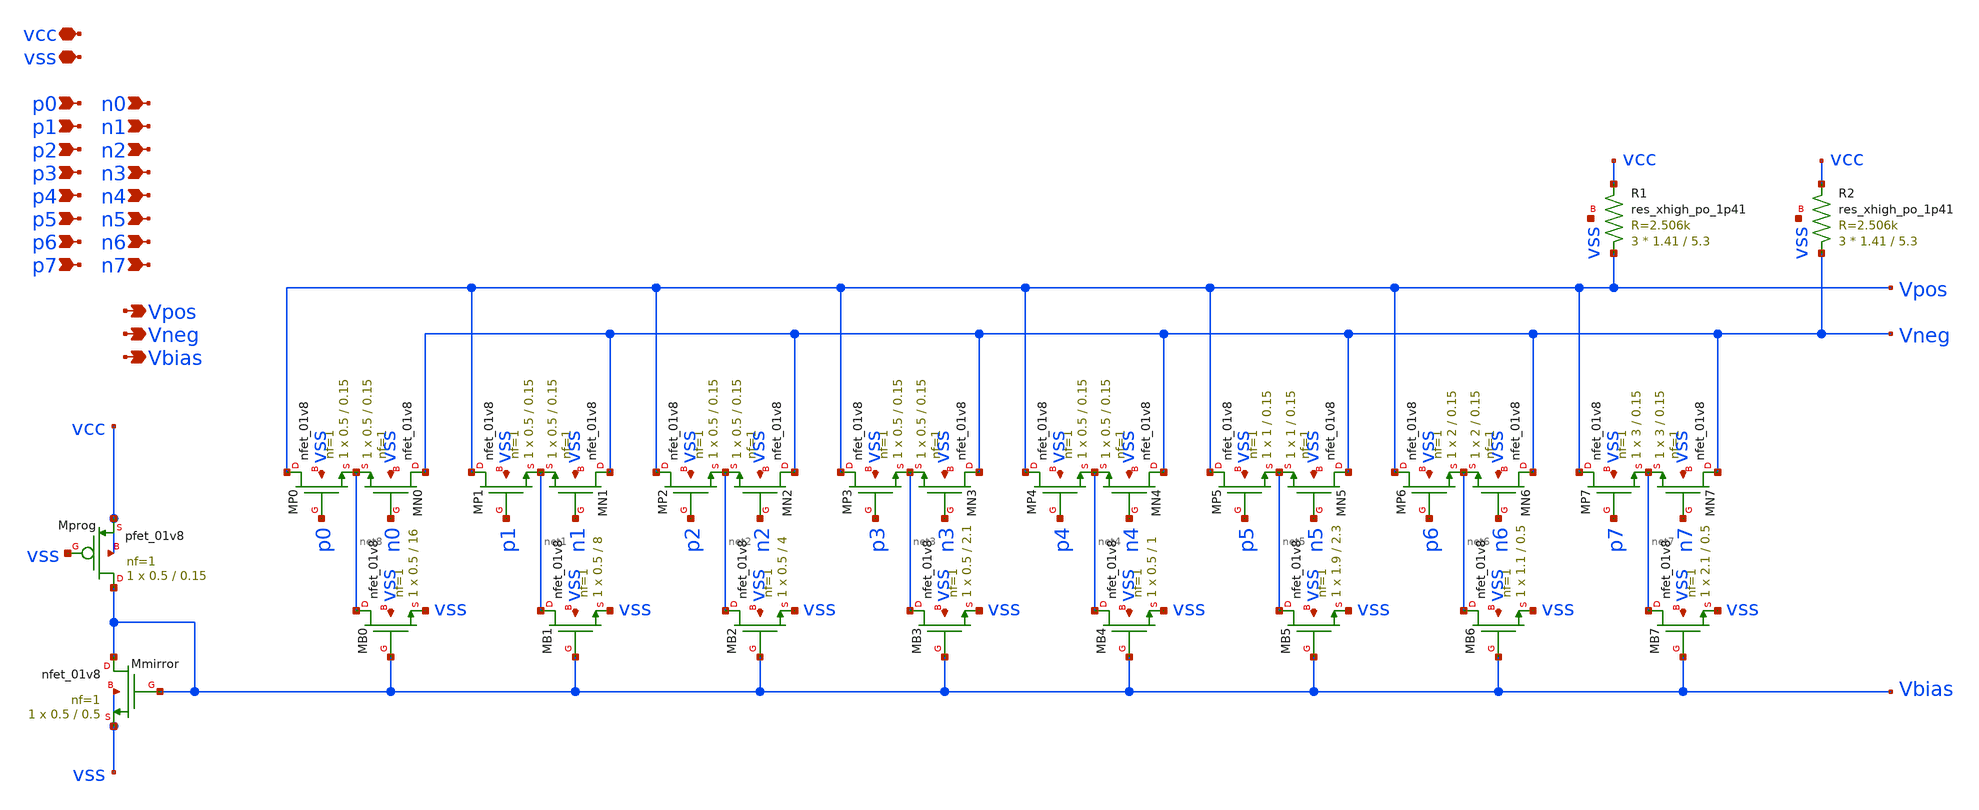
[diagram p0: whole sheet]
** sch_path: xschem/csdac.sch
**.subckt csdac vcc vss p0 n0 p1 n1 p2 n2 p3 n3 p4 n4 p5 n5 p6 n6 p7 n7 Vpos Vneg Vbias
*.iopin vcc
*.iopin vss
*.ipin p0
*.ipin n0
*.ipin p1
*.ipin n1
*.ipin p2
*.ipin n2
*.ipin p3
*.ipin n3
*.ipin p4
*.ipin n4
*.ipin p5
*.ipin n5
*.ipin p6
*.ipin n6
*.ipin p7
*.ipin n7
*.opin Vpos
*.opin Vneg
*.opin Vbias
XMprog Vbias vss vcc vcc sky130_fd_pr__pfet_01v8 L=0.15 W=0.5 nf=1 ad='int((nf+1)/2) * W/nf * 0.29' as='int((nf+2)/2) * W/nf * 0.29'
+ pd='2*int((nf+1)/2) * (W/nf + 0.29)' ps='2*int((nf+2)/2) * (W/nf + 0.29)' nrd='0.29 / W' nrs='0.29 / W'
+ sa=0 sb=0 sd=0 mult=1 m=1
XMmirror Vbias Vbias vss vss sky130_fd_pr__nfet_01v8 L=0.5 W=0.5 nf=1 ad='int((nf+1)/2) * W/nf * 0.29'
+ as='int((nf+2)/2) * W/nf * 0.29' pd='2*int((nf+1)/2) * (W/nf + 0.29)' ps='2*int((nf+2)/2) * (W/nf + 0.29)'
+ nrd='0.29 / W' nrs='0.29 / W' sa=0 sb=0 sd=0 mult=1 m=1
XMB0 net8 Vbias vss vss sky130_fd_pr__nfet_01v8 L=16 W=0.5 nf=1 ad='int((nf+1)/2) * W/nf * 0.29' as='int((nf+2)/2) * W/nf * 0.29'
+ pd='2*int((nf+1)/2) * (W/nf + 0.29)' ps='2*int((nf+2)/2) * (W/nf + 0.29)' nrd='0.29 / W' nrs='0.29 / W'
+ sa=0 sb=0 sd=0 mult=1 m=1
XMP0 Vpos p0 net8 vss sky130_fd_pr__nfet_01v8 L=0.15 W=0.5 nf=1 ad='int((nf+1)/2) * W/nf * 0.29' as='int((nf+2)/2) * W/nf * 0.29'
+ pd='2*int((nf+1)/2) * (W/nf + 0.29)' ps='2*int((nf+2)/2) * (W/nf + 0.29)' nrd='0.29 / W' nrs='0.29 / W'
+ sa=0 sb=0 sd=0 mult=1 m=1
XMN0 Vneg n0 net8 vss sky130_fd_pr__nfet_01v8 L=0.15 W=0.5 nf=1 ad='int((nf+1)/2) * W/nf * 0.29' as='int((nf+2)/2) * W/nf * 0.29'
+ pd='2*int((nf+1)/2) * (W/nf + 0.29)' ps='2*int((nf+2)/2) * (W/nf + 0.29)' nrd='0.29 / W' nrs='0.29 / W'
+ sa=0 sb=0 sd=0 mult=1 m=1
XMB1 net1 Vbias vss vss sky130_fd_pr__nfet_01v8 L=8 W=0.5 nf=1 ad='int((nf+1)/2) * W/nf * 0.29' as='int((nf+2)/2) * W/nf * 0.29'
+ pd='2*int((nf+1)/2) * (W/nf + 0.29)' ps='2*int((nf+2)/2) * (W/nf + 0.29)' nrd='0.29 / W' nrs='0.29 / W'
+ sa=0 sb=0 sd=0 mult=1 m=1
XMP1 Vpos p1 net1 vss sky130_fd_pr__nfet_01v8 L=0.15 W=0.5 nf=1 ad='int((nf+1)/2) * W/nf * 0.29' as='int((nf+2)/2) * W/nf * 0.29'
+ pd='2*int((nf+1)/2) * (W/nf + 0.29)' ps='2*int((nf+2)/2) * (W/nf + 0.29)' nrd='0.29 / W' nrs='0.29 / W'
+ sa=0 sb=0 sd=0 mult=1 m=1
XMN1 Vneg n1 net1 vss sky130_fd_pr__nfet_01v8 L=0.15 W=0.5 nf=1 ad='int((nf+1)/2) * W/nf * 0.29' as='int((nf+2)/2) * W/nf * 0.29'
+ pd='2*int((nf+1)/2) * (W/nf + 0.29)' ps='2*int((nf+2)/2) * (W/nf + 0.29)' nrd='0.29 / W' nrs='0.29 / W'
+ sa=0 sb=0 sd=0 mult=1 m=1
XMB2 net2 Vbias vss vss sky130_fd_pr__nfet_01v8 L=4 W=0.5 nf=1 ad='int((nf+1)/2) * W/nf * 0.29' as='int((nf+2)/2) * W/nf * 0.29'
+ pd='2*int((nf+1)/2) * (W/nf + 0.29)' ps='2*int((nf+2)/2) * (W/nf + 0.29)' nrd='0.29 / W' nrs='0.29 / W'
+ sa=0 sb=0 sd=0 mult=1 m=1
XMP2 Vpos p2 net2 vss sky130_fd_pr__nfet_01v8 L=0.15 W=0.5 nf=1 ad='int((nf+1)/2) * W/nf * 0.29' as='int((nf+2)/2) * W/nf * 0.29'
+ pd='2*int((nf+1)/2) * (W/nf + 0.29)' ps='2*int((nf+2)/2) * (W/nf + 0.29)' nrd='0.29 / W' nrs='0.29 / W'
+ sa=0 sb=0 sd=0 mult=1 m=1
XMN2 Vneg n2 net2 vss sky130_fd_pr__nfet_01v8 L=0.15 W=0.5 nf=1 ad='int((nf+1)/2) * W/nf * 0.29' as='int((nf+2)/2) * W/nf * 0.29'
+ pd='2*int((nf+1)/2) * (W/nf + 0.29)' ps='2*int((nf+2)/2) * (W/nf + 0.29)' nrd='0.29 / W' nrs='0.29 / W'
+ sa=0 sb=0 sd=0 mult=1 m=1
XMB3 net3 Vbias vss vss sky130_fd_pr__nfet_01v8 L=2.1 W=0.5 nf=1 ad='int((nf+1)/2) * W/nf * 0.29' as='int((nf+2)/2) * W/nf * 0.29'
+ pd='2*int((nf+1)/2) * (W/nf + 0.29)' ps='2*int((nf+2)/2) * (W/nf + 0.29)' nrd='0.29 / W' nrs='0.29 / W'
+ sa=0 sb=0 sd=0 mult=1 m=1
XMP3 Vpos p3 net3 vss sky130_fd_pr__nfet_01v8 L=0.15 W=0.5 nf=1 ad='int((nf+1)/2) * W/nf * 0.29' as='int((nf+2)/2) * W/nf * 0.29'
+ pd='2*int((nf+1)/2) * (W/nf + 0.29)' ps='2*int((nf+2)/2) * (W/nf + 0.29)' nrd='0.29 / W' nrs='0.29 / W'
+ sa=0 sb=0 sd=0 mult=1 m=1
XMN3 Vneg n3 net3 vss sky130_fd_pr__nfet_01v8 L=0.15 W=0.5 nf=1 ad='int((nf+1)/2) * W/nf * 0.29' as='int((nf+2)/2) * W/nf * 0.29'
+ pd='2*int((nf+1)/2) * (W/nf + 0.29)' ps='2*int((nf+2)/2) * (W/nf + 0.29)' nrd='0.29 / W' nrs='0.29 / W'
+ sa=0 sb=0 sd=0 mult=1 m=1
XMB4 net4 Vbias vss vss sky130_fd_pr__nfet_01v8 L=1 W=0.5 nf=1 ad='int((nf+1)/2) * W/nf * 0.29' as='int((nf+2)/2) * W/nf * 0.29'
+ pd='2*int((nf+1)/2) * (W/nf + 0.29)' ps='2*int((nf+2)/2) * (W/nf + 0.29)' nrd='0.29 / W' nrs='0.29 / W'
+ sa=0 sb=0 sd=0 mult=1 m=1
XMP4 Vpos p4 net4 vss sky130_fd_pr__nfet_01v8 L=0.15 W=0.5 nf=1 ad='int((nf+1)/2) * W/nf * 0.29' as='int((nf+2)/2) * W/nf * 0.29'
+ pd='2*int((nf+1)/2) * (W/nf + 0.29)' ps='2*int((nf+2)/2) * (W/nf + 0.29)' nrd='0.29 / W' nrs='0.29 / W'
+ sa=0 sb=0 sd=0 mult=1 m=1
XMN4 Vneg n4 net4 vss sky130_fd_pr__nfet_01v8 L=0.15 W=0.5 nf=1 ad='int((nf+1)/2) * W/nf * 0.29' as='int((nf+2)/2) * W/nf * 0.29'
+ pd='2*int((nf+1)/2) * (W/nf + 0.29)' ps='2*int((nf+2)/2) * (W/nf + 0.29)' nrd='0.29 / W' nrs='0.29 / W'
+ sa=0 sb=0 sd=0 mult=1 m=1
XMB5 net5 Vbias vss vss sky130_fd_pr__nfet_01v8 L=2.3 W=1.9 nf=1 ad='int((nf+1)/2) * W/nf * 0.29' as='int((nf+2)/2) * W/nf * 0.29'
+ pd='2*int((nf+1)/2) * (W/nf + 0.29)' ps='2*int((nf+2)/2) * (W/nf + 0.29)' nrd='0.29 / W' nrs='0.29 / W'
+ sa=0 sb=0 sd=0 mult=1 m=1
XMP5 Vpos p5 net5 vss sky130_fd_pr__nfet_01v8 L=0.15 W=1 nf=1 ad='int((nf+1)/2) * W/nf * 0.29' as='int((nf+2)/2) * W/nf * 0.29'
+ pd='2*int((nf+1)/2) * (W/nf + 0.29)' ps='2*int((nf+2)/2) * (W/nf + 0.29)' nrd='0.29 / W' nrs='0.29 / W'
+ sa=0 sb=0 sd=0 mult=1 m=1
XMN5 Vneg n5 net5 vss sky130_fd_pr__nfet_01v8 L=0.15 W=1 nf=1 ad='int((nf+1)/2) * W/nf * 0.29' as='int((nf+2)/2) * W/nf * 0.29'
+ pd='2*int((nf+1)/2) * (W/nf + 0.29)' ps='2*int((nf+2)/2) * (W/nf + 0.29)' nrd='0.29 / W' nrs='0.29 / W'
+ sa=0 sb=0 sd=0 mult=1 m=1
XMB6 net6 Vbias vss vss sky130_fd_pr__nfet_01v8 L=0.5 W=1.1 nf=1 ad='int((nf+1)/2) * W/nf * 0.29' as='int((nf+2)/2) * W/nf * 0.29'
+ pd='2*int((nf+1)/2) * (W/nf + 0.29)' ps='2*int((nf+2)/2) * (W/nf + 0.29)' nrd='0.29 / W' nrs='0.29 / W'
+ sa=0 sb=0 sd=0 mult=1 m=1
XMP6 Vpos p6 net6 vss sky130_fd_pr__nfet_01v8 L=0.15 W=2 nf=1 ad='int((nf+1)/2) * W/nf * 0.29' as='int((nf+2)/2) * W/nf * 0.29'
+ pd='2*int((nf+1)/2) * (W/nf + 0.29)' ps='2*int((nf+2)/2) * (W/nf + 0.29)' nrd='0.29 / W' nrs='0.29 / W'
+ sa=0 sb=0 sd=0 mult=1 m=1
XMN6 Vneg n6 net6 vss sky130_fd_pr__nfet_01v8 L=0.15 W=2 nf=1 ad='int((nf+1)/2) * W/nf * 0.29' as='int((nf+2)/2) * W/nf * 0.29'
+ pd='2*int((nf+1)/2) * (W/nf + 0.29)' ps='2*int((nf+2)/2) * (W/nf + 0.29)' nrd='0.29 / W' nrs='0.29 / W'
+ sa=0 sb=0 sd=0 mult=1 m=1
XMB7 net7 Vbias vss vss sky130_fd_pr__nfet_01v8 L=0.5 W=2.1 nf=1 ad='int((nf+1)/2) * W/nf * 0.29' as='int((nf+2)/2) * W/nf * 0.29'
+ pd='2*int((nf+1)/2) * (W/nf + 0.29)' ps='2*int((nf+2)/2) * (W/nf + 0.29)' nrd='0.29 / W' nrs='0.29 / W'
+ sa=0 sb=0 sd=0 mult=1 m=1
XMP7 Vpos p7 net7 vss sky130_fd_pr__nfet_01v8 L=0.15 W=3 nf=1 ad='int((nf+1)/2) * W/nf * 0.29' as='int((nf+2)/2) * W/nf * 0.29'
+ pd='2*int((nf+1)/2) * (W/nf + 0.29)' ps='2*int((nf+2)/2) * (W/nf + 0.29)' nrd='0.29 / W' nrs='0.29 / W'
+ sa=0 sb=0 sd=0 mult=1 m=1
XMN7 Vneg n7 net7 vss sky130_fd_pr__nfet_01v8 L=0.15 W=3 nf=1 ad='int((nf+1)/2) * W/nf * 0.29' as='int((nf+2)/2) * W/nf * 0.29'
+ pd='2*int((nf+1)/2) * (W/nf + 0.29)' ps='2*int((nf+2)/2) * (W/nf + 0.29)' nrd='0.29 / W' nrs='0.29 / W'
+ sa=0 sb=0 sd=0 mult=1 m=1
XR1 Vpos vcc vss sky130_fd_pr__res_xhigh_po_1p41 L=5.3 mult=3 m=3
XR2 Vneg vcc vss sky130_fd_pr__res_xhigh_po_1p41 L=5.3 mult=3 m=3
**.ends
.end
